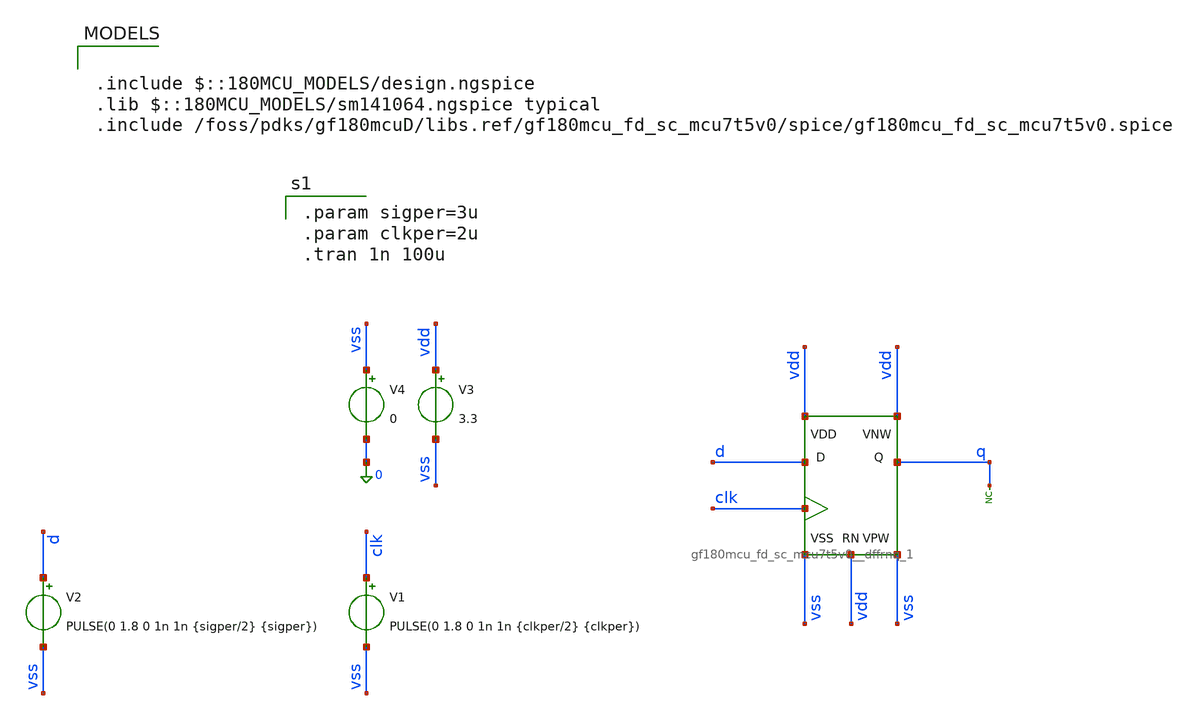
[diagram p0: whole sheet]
** sch_path: xschem/archive/mcu7t5v0/gf180mcu_fd_sc_mcu7t5v0__dffrnq_1_test.sch
**.subckt gf180mcu_fd_sc_mcu7t5v0__dffrnq_1_test
x1 d vdd clk q vdd vdd vss vss gf180mcu_fd_sc_mcu7t5v0__dffrnq_1
V1 clk vss PULSE(0 1.8 0 1n 1n {clkper/2} {clkper})
V3 vdd vss 3.3
V4 vss 0 0
V2 d vss PULSE(0 1.8 0 1n 1n {sigper/2} {sigper})
* noconn q
**** begin user architecture code

.param sigper=3u
.param clkper=2u
.tran 1n 100u


.include $::180MCU_MODELS/design.ngspice
.lib $::180MCU_MODELS/sm141064.ngspice typical
.include /foss/pdks/gf180mcuD/libs.ref/gf180mcu_fd_sc_mcu7t5v0/spice/gf180mcu_fd_sc_mcu7t5v0.spice

**** end user architecture code
**.ends
.end
